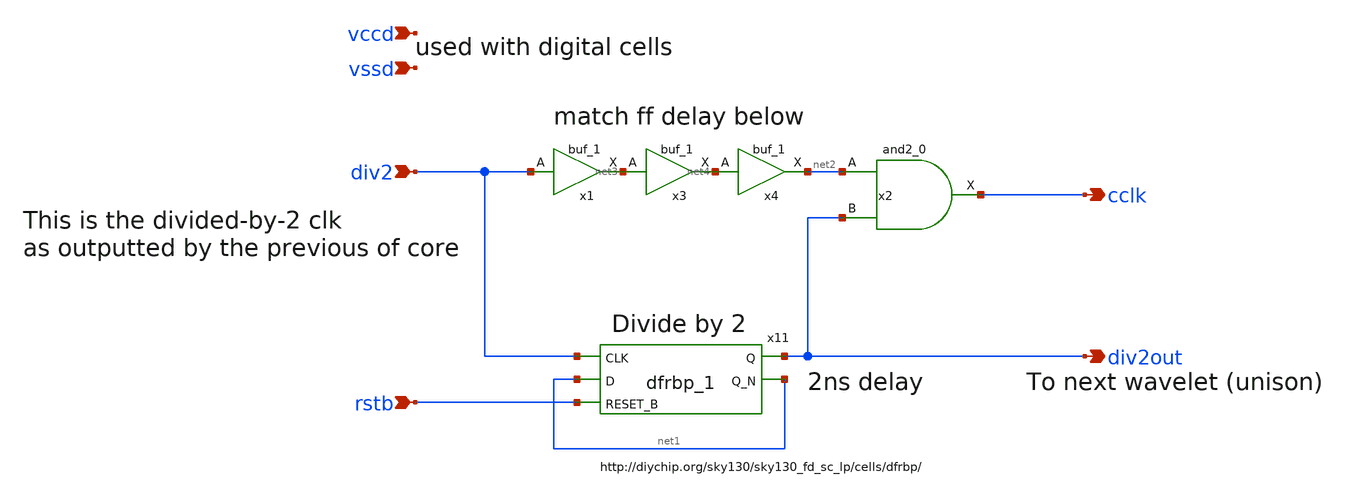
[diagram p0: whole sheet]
** sch_path: xschem/clkgen/dig_div2.sch
**.subckt dig_div2 div2 rstb cclk div2out vccd vssd
*.ipin div2
*.ipin rstb
*.opin cclk
*.opin div2out
*.ipin vccd
*.ipin vssd
x11 div2 net1 rstb vssd vssd vccd vccd div2out net1 sky130_fd_sc_hd__dfrbp_1
x2 net2 div2out vssd vssd vccd vccd cclk sky130_fd_sc_hd__and2_0
x1 div2 vssd vssd vccd vccd net3 sky130_fd_sc_hd__buf_1
x3 net3 vssd vssd vccd vccd net4 sky130_fd_sc_hd__buf_1
x4 net4 vssd vssd vccd vccd net2 sky130_fd_sc_hd__buf_1
**.ends
.end
